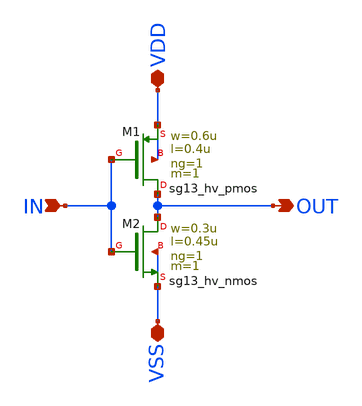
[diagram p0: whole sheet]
** sch_path: real_circuit/real_inv.sch
**.subckt real_inv VDD VSS IN OUT
*.iopin VDD
*.iopin VSS
*.ipin IN
*.opin OUT
XM1 OUT IN VDD VDD sg13_hv_pmos w=0.6u l=0.4u ng=1 m=1 mm_ok=1
XM2 OUT IN VSS VSS sg13_hv_nmos w=0.3u l=0.45u ng=1 m=1 mm_ok=1
**.ends
.end
